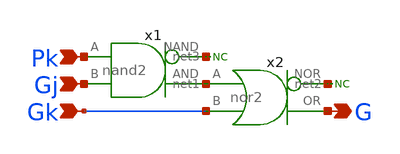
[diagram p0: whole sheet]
** sch_path: elements/ks_grey.sch
**.subckt ks_grey G Pk Gj Gk
*.opin G
*.ipin Pk
*.ipin Gj
*.ipin Gk
x2 net1 G Gk net2 nor2
* noconn #net2
x1 net3 net1 Pk Gj nand2
* noconn #net3
**.ends
.end
